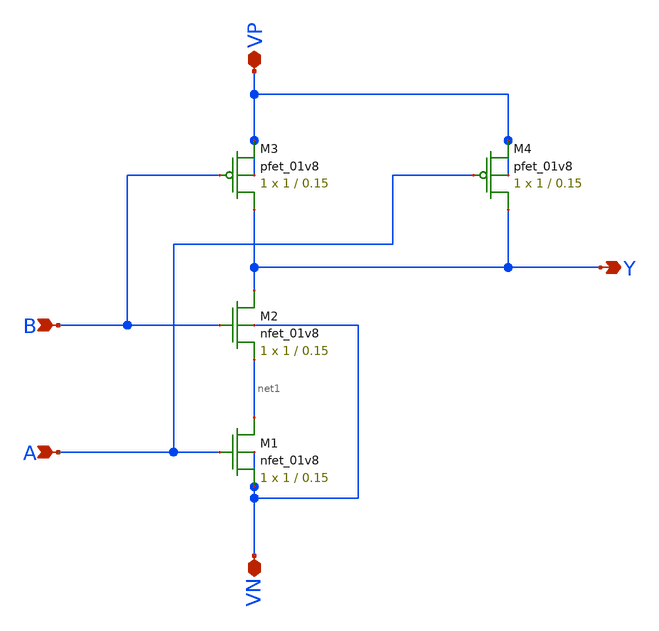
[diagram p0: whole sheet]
** sch_path: Mini_Project_1/Schematic/NAND_Gate.sch
**.subckt NAND_Gate A Y VP VN B
*.ipin A
*.opin Y
*.iopin VP
*.iopin VN
*.ipin B
XM1 net1 A VN VN sky130_fd_pr__nfet_01v8 L=0.15 W=1 nf=1 ad='int((nf+1)/2) * W/nf * 0.29' as='int((nf+2)/2) * W/nf * 0.29'
+ pd='2*int((nf+1)/2) * (W/nf + 0.29)' ps='2*int((nf+2)/2) * (W/nf + 0.29)' nrd='0.29 / W' nrs='0.29 / W'
+ sa=0 sb=0 sd=0 mult=1 m=1
XM2 Y B net1 VN sky130_fd_pr__nfet_01v8 L=0.15 W=1 nf=1 ad='int((nf+1)/2) * W/nf * 0.29' as='int((nf+2)/2) * W/nf * 0.29'
+ pd='2*int((nf+1)/2) * (W/nf + 0.29)' ps='2*int((nf+2)/2) * (W/nf + 0.29)' nrd='0.29 / W' nrs='0.29 / W'
+ sa=0 sb=0 sd=0 mult=1 m=1
XM3 Y B VP VP sky130_fd_pr__pfet_01v8 L=0.15 W=1 nf=1 ad='int((nf+1)/2) * W/nf * 0.29' as='int((nf+2)/2) * W/nf * 0.29'
+ pd='2*int((nf+1)/2) * (W/nf + 0.29)' ps='2*int((nf+2)/2) * (W/nf + 0.29)' nrd='0.29 / W' nrs='0.29 / W'
+ sa=0 sb=0 sd=0 mult=1 m=1
XM4 Y A VP VP sky130_fd_pr__pfet_01v8 L=0.15 W=1 nf=1 ad='int((nf+1)/2) * W/nf * 0.29' as='int((nf+2)/2) * W/nf * 0.29'
+ pd='2*int((nf+1)/2) * (W/nf + 0.29)' ps='2*int((nf+2)/2) * (W/nf + 0.29)' nrd='0.29 / W' nrs='0.29 / W'
+ sa=0 sb=0 sd=0 mult=1 m=1
**.ends
.end
